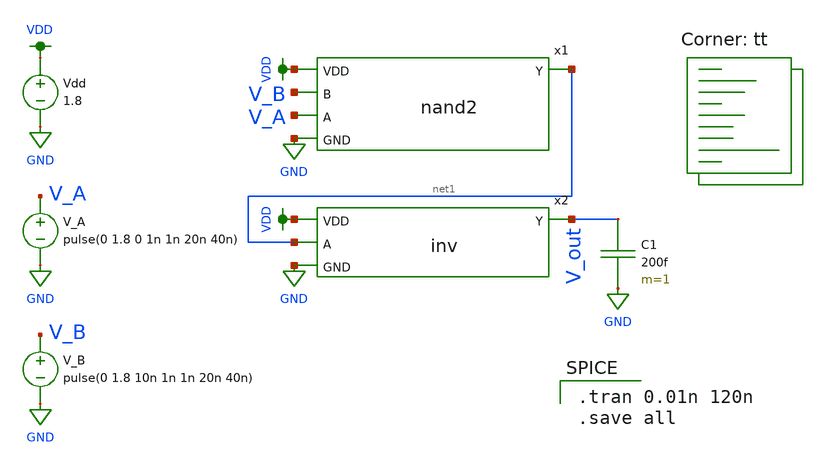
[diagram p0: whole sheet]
** sch_path: MP1/xschem/and.sch
**.subckt and
C1 V_out GND 200f m=1
Vdd VDD GND 1.8
V_A V_A GND pulse(0 1.8 0 1n 1n 20n 40n)
V_B V_B GND pulse(0 1.8 10n 1n 1n 20n 40n)
x2 VDD net1 V_out GND inv
x1 VDD net1 V_B V_A GND nand2
**** begin user architecture code

.tran 0.01n 120n
.save all

.lib $::SKYWATER_MODELS/sky130.lib.spice tt
**** end user architecture code
**.ends

* expanding   symbol:  /home/madvlsi/Desktop/MP1/xschem/inv.sym # of pins=4
** sym_path: MP2/xschem/inv.sym
** sch_path: MP2/xschem/inv.sch
.subckt inv VDD A Y GND
*.ipin A
*.opin Y
*.ipin VDD
*.ipin GND
XM1 Y A GND GND sky130_fd_pr__nfet_01v8 L=0.15 W=1 nf=1 ad='int((nf+1)/2) * W/nf * 0.29' as='int((nf+2)/2) * W/nf * 0.29'
+ pd='2*int((nf+1)/2) * (W/nf + 0.29)' ps='2*int((nf+2)/2) * (W/nf + 0.29)' nrd='0.29 / W' nrs='0.29 / W'
+ sa=0 sb=0 sd=0 mult=1 m=1
XM2 Y A VDD VDD sky130_fd_pr__pfet_01v8 L=0.15 W=1 nf=1 ad='int((nf+1)/2) * W/nf * 0.29' as='int((nf+2)/2) * W/nf * 0.29'
+ pd='2*int((nf+1)/2) * (W/nf + 0.29)' ps='2*int((nf+2)/2) * (W/nf + 0.29)' nrd='0.29 / W' nrs='0.29 / W'
+ sa=0 sb=0 sd=0 mult=1 m=1
.ends


* expanding   symbol:  /home/madvlsi/Desktop/MP1/xschem/nand2.sym # of pins=5
** sym_path: MP1/xschem/nand2.sym
** sch_path: MP1/xschem/nand2.sch
.subckt nand2 VDD Y B A GND
*.ipin A
*.ipin B
*.opin Y
*.ipin VDD
*.ipin GND
XM1 VDD A Y VDD sky130_fd_pr__pfet_01v8 L=0.4 W=1 nf=1 ad='int((nf+1)/2) * W/nf * 0.29' as='int((nf+2)/2) * W/nf * 0.29'
+ pd='2*int((nf+1)/2) * (W/nf + 0.29)' ps='2*int((nf+2)/2) * (W/nf + 0.29)' nrd='0.29 / W' nrs='0.29 / W'
+ sa=0 sb=0 sd=0 mult=1 m=1
XM2 Y B VDD VDD sky130_fd_pr__pfet_01v8 L=0.4 W=1 nf=1 ad='int((nf+1)/2) * W/nf * 0.29' as='int((nf+2)/2) * W/nf * 0.29'
+ pd='2*int((nf+1)/2) * (W/nf + 0.29)' ps='2*int((nf+2)/2) * (W/nf + 0.29)' nrd='0.29 / W' nrs='0.29 / W'
+ sa=0 sb=0 sd=0 mult=1 m=1
XM3 Y B net1 GND sky130_fd_pr__nfet_01v8 L=0.4 W=1 nf=1 ad='int((nf+1)/2) * W/nf * 0.29' as='int((nf+2)/2) * W/nf * 0.29'
+ pd='2*int((nf+1)/2) * (W/nf + 0.29)' ps='2*int((nf+2)/2) * (W/nf + 0.29)' nrd='0.29 / W' nrs='0.29 / W'
+ sa=0 sb=0 sd=0 mult=1 m=1
XM4 net1 A GND GND sky130_fd_pr__nfet_01v8 L=0.4 W=1 nf=1 ad='int((nf+1)/2) * W/nf * 0.29' as='int((nf+2)/2) * W/nf * 0.29'
+ pd='2*int((nf+1)/2) * (W/nf + 0.29)' ps='2*int((nf+2)/2) * (W/nf + 0.29)' nrd='0.29 / W' nrs='0.29 / W'
+ sa=0 sb=0 sd=0 mult=1 m=1
.ends

.GLOBAL VDD
.GLOBAL GND
.end
